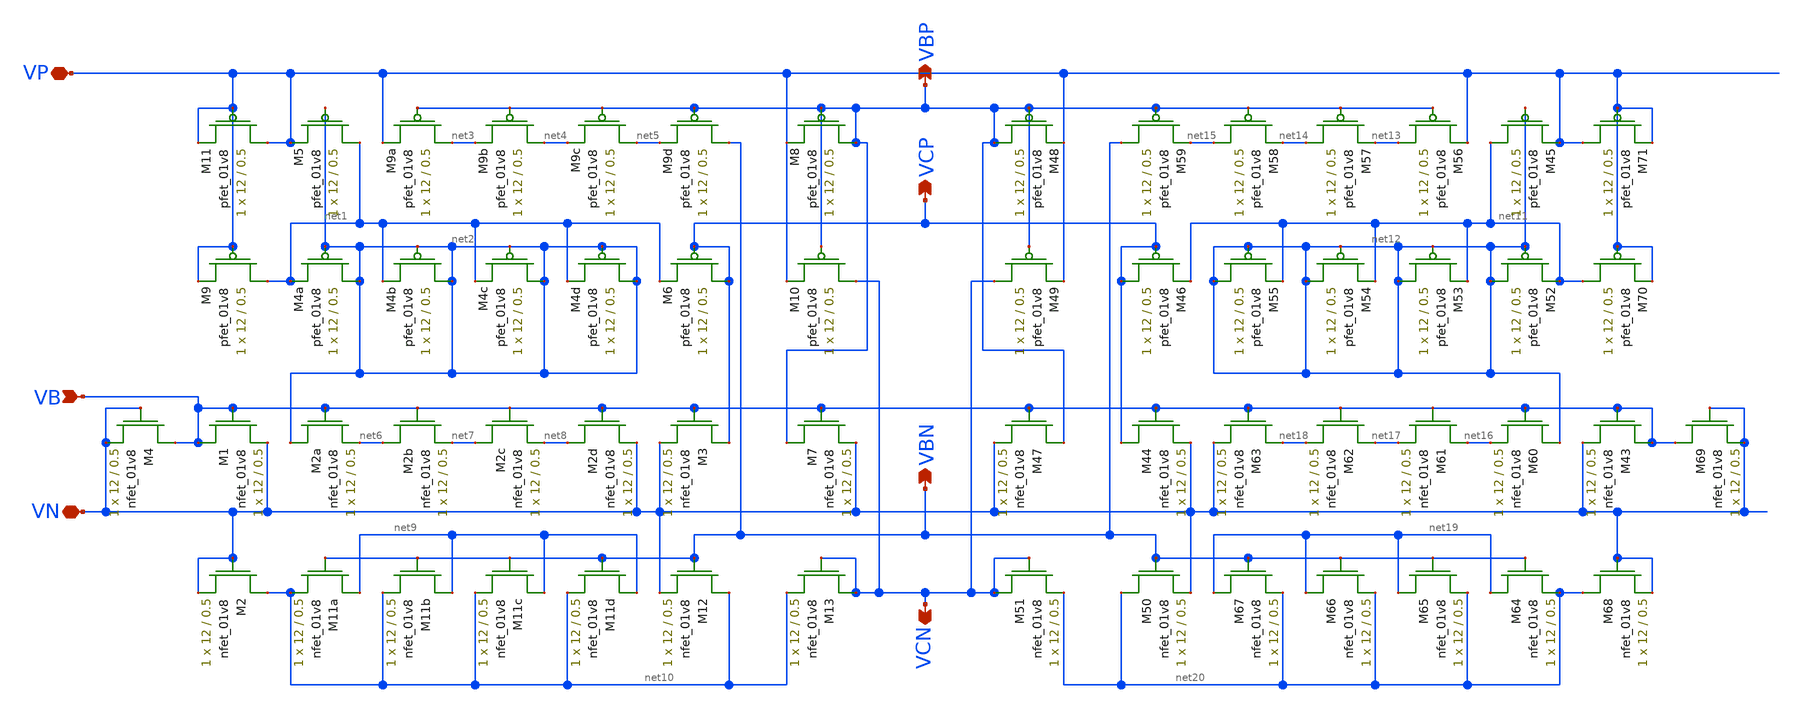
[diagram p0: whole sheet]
** sch_path: mp3/bias_gen/bias_gen_LDS_v2.sch
**.subckt bias_gen_LDS_v2 VN VP VCN VCP VBP VB VBN
*.iopin VN
*.iopin VP
*.opin VCN
*.opin VCP
*.opin VBP
*.ipin VB
*.opin VBN
XM1 VB VB VN VN sky130_fd_pr__nfet_01v8 L=0.5 W=12 nf=1 ad='int((nf+1)/2) * W/nf * 0.29' as='int((nf+2)/2) * W/nf * 0.29'
+ pd='2*int((nf+1)/2) * (W/nf + 0.29)' ps='2*int((nf+2)/2) * (W/nf + 0.29)' nrd='0.29 / W' nrs='0.29 / W'
+ sa=0 sb=0 sd=0 mult=1 m=1
XM3 VCP VB VN VN sky130_fd_pr__nfet_01v8 L=0.5 W=12 nf=1 ad='int((nf+1)/2) * W/nf * 0.29' as='int((nf+2)/2) * W/nf * 0.29'
+ pd='2*int((nf+1)/2) * (W/nf + 0.29)' ps='2*int((nf+2)/2) * (W/nf + 0.29)' nrd='0.29 / W' nrs='0.29 / W'
+ sa=0 sb=0 sd=0 mult=1 m=1
XM5 net1 net2 VP VP sky130_fd_pr__pfet_01v8 L=0.5 W=12 nf=1 ad='int((nf+1)/2) * W/nf * 0.29' as='int((nf+2)/2) * W/nf * 0.29'
+ pd='2*int((nf+1)/2) * (W/nf + 0.29)' ps='2*int((nf+2)/2) * (W/nf + 0.29)' nrd='0.29 / W' nrs='0.29 / W'
+ sa=0 sb=0 sd=0 mult=1 m=1
XM6 VCP VCP net1 VP sky130_fd_pr__pfet_01v8 L=0.5 W=12 nf=1 ad='int((nf+1)/2) * W/nf * 0.29' as='int((nf+2)/2) * W/nf * 0.29'
+ pd='2*int((nf+1)/2) * (W/nf + 0.29)' ps='2*int((nf+2)/2) * (W/nf + 0.29)' nrd='0.29 / W' nrs='0.29 / W'
+ sa=0 sb=0 sd=0 mult=1 m=1
XM7 VBP VB VN VN sky130_fd_pr__nfet_01v8 L=0.5 W=12 nf=1 ad='int((nf+1)/2) * W/nf * 0.29' as='int((nf+2)/2) * W/nf * 0.29'
+ pd='2*int((nf+1)/2) * (W/nf + 0.29)' ps='2*int((nf+2)/2) * (W/nf + 0.29)' nrd='0.29 / W' nrs='0.29 / W'
+ sa=0 sb=0 sd=0 mult=1 m=1
XM8 VBP VBP VP VP sky130_fd_pr__pfet_01v8 L=0.5 W=12 nf=1 ad='int((nf+1)/2) * W/nf * 0.29' as='int((nf+2)/2) * W/nf * 0.29'
+ pd='2*int((nf+1)/2) * (W/nf + 0.29)' ps='2*int((nf+2)/2) * (W/nf + 0.29)' nrd='0.29 / W' nrs='0.29 / W'
+ sa=0 sb=0 sd=0 mult=1 m=1
XM10 VCN VBP VP VP sky130_fd_pr__pfet_01v8 L=0.5 W=12 nf=1 ad='int((nf+1)/2) * W/nf * 0.29' as='int((nf+2)/2) * W/nf * 0.29'
+ pd='2*int((nf+1)/2) * (W/nf + 0.29)' ps='2*int((nf+2)/2) * (W/nf + 0.29)' nrd='0.29 / W' nrs='0.29 / W'
+ sa=0 sb=0 sd=0 mult=1 m=1
XM12 net10 VBN VN VN sky130_fd_pr__nfet_01v8 L=0.5 W=12 nf=1 ad='int((nf+1)/2) * W/nf * 0.29' as='int((nf+2)/2) * W/nf * 0.29'
+ pd='2*int((nf+1)/2) * (W/nf + 0.29)' ps='2*int((nf+2)/2) * (W/nf + 0.29)' nrd='0.29 / W' nrs='0.29 / W'
+ sa=0 sb=0 sd=0 mult=1 m=1
XM13 VCN VCN net10 VN sky130_fd_pr__nfet_01v8 L=0.5 W=12 nf=1 ad='int((nf+1)/2) * W/nf * 0.29' as='int((nf+2)/2) * W/nf * 0.29'
+ pd='2*int((nf+1)/2) * (W/nf + 0.29)' ps='2*int((nf+2)/2) * (W/nf + 0.29)' nrd='0.29 / W' nrs='0.29 / W'
+ sa=0 sb=0 sd=0 mult=1 m=1
XM4a net2 net2 net1 VP sky130_fd_pr__pfet_01v8 L=0.5 W=12 nf=1 ad='int((nf+1)/2) * W/nf * 0.29' as='int((nf+2)/2) * W/nf * 0.29'
+ pd='2*int((nf+1)/2) * (W/nf + 0.29)' ps='2*int((nf+2)/2) * (W/nf + 0.29)' nrd='0.29 / W' nrs='0.29 / W'
+ sa=0 sb=0 sd=0 mult=1 m=1
XM4b net2 net2 net1 VP sky130_fd_pr__pfet_01v8 L=0.5 W=12 nf=1 ad='int((nf+1)/2) * W/nf * 0.29' as='int((nf+2)/2) * W/nf * 0.29'
+ pd='2*int((nf+1)/2) * (W/nf + 0.29)' ps='2*int((nf+2)/2) * (W/nf + 0.29)' nrd='0.29 / W' nrs='0.29 / W'
+ sa=0 sb=0 sd=0 mult=1 m=1
XM4c net2 net2 net1 VP sky130_fd_pr__pfet_01v8 L=0.5 W=12 nf=1 ad='int((nf+1)/2) * W/nf * 0.29' as='int((nf+2)/2) * W/nf * 0.29'
+ pd='2*int((nf+1)/2) * (W/nf + 0.29)' ps='2*int((nf+2)/2) * (W/nf + 0.29)' nrd='0.29 / W' nrs='0.29 / W'
+ sa=0 sb=0 sd=0 mult=1 m=1
XM4d net2 net2 net1 VP sky130_fd_pr__pfet_01v8 L=0.5 W=12 nf=1 ad='int((nf+1)/2) * W/nf * 0.29' as='int((nf+2)/2) * W/nf * 0.29'
+ pd='2*int((nf+1)/2) * (W/nf + 0.29)' ps='2*int((nf+2)/2) * (W/nf + 0.29)' nrd='0.29 / W' nrs='0.29 / W'
+ sa=0 sb=0 sd=0 mult=1 m=1
XM9a net3 VBP VP VP sky130_fd_pr__pfet_01v8 L=0.5 W=12 nf=1 ad='int((nf+1)/2) * W/nf * 0.29' as='int((nf+2)/2) * W/nf * 0.29'
+ pd='2*int((nf+1)/2) * (W/nf + 0.29)' ps='2*int((nf+2)/2) * (W/nf + 0.29)' nrd='0.29 / W' nrs='0.29 / W'
+ sa=0 sb=0 sd=0 mult=1 m=1
XM9b net4 VBP net3 VP sky130_fd_pr__pfet_01v8 L=0.5 W=12 nf=1 ad='int((nf+1)/2) * W/nf * 0.29' as='int((nf+2)/2) * W/nf * 0.29'
+ pd='2*int((nf+1)/2) * (W/nf + 0.29)' ps='2*int((nf+2)/2) * (W/nf + 0.29)' nrd='0.29 / W' nrs='0.29 / W'
+ sa=0 sb=0 sd=0 mult=1 m=1
XM9c net5 VBP net4 VP sky130_fd_pr__pfet_01v8 L=0.5 W=12 nf=1 ad='int((nf+1)/2) * W/nf * 0.29' as='int((nf+2)/2) * W/nf * 0.29'
+ pd='2*int((nf+1)/2) * (W/nf + 0.29)' ps='2*int((nf+2)/2) * (W/nf + 0.29)' nrd='0.29 / W' nrs='0.29 / W'
+ sa=0 sb=0 sd=0 mult=1 m=1
XM9d VBN VBP net5 VP sky130_fd_pr__pfet_01v8 L=0.5 W=12 nf=1 ad='int((nf+1)/2) * W/nf * 0.29' as='int((nf+2)/2) * W/nf * 0.29'
+ pd='2*int((nf+1)/2) * (W/nf + 0.29)' ps='2*int((nf+2)/2) * (W/nf + 0.29)' nrd='0.29 / W' nrs='0.29 / W'
+ sa=0 sb=0 sd=0 mult=1 m=1
XM2a net2 VB net6 VN sky130_fd_pr__nfet_01v8 L=0.5 W=12 nf=1 ad='int((nf+1)/2) * W/nf * 0.29' as='int((nf+2)/2) * W/nf * 0.29'
+ pd='2*int((nf+1)/2) * (W/nf + 0.29)' ps='2*int((nf+2)/2) * (W/nf + 0.29)' nrd='0.29 / W' nrs='0.29 / W'
+ sa=0 sb=0 sd=0 mult=1 m=1
XM2b net6 VB net7 VN sky130_fd_pr__nfet_01v8 L=0.5 W=12 nf=1 ad='int((nf+1)/2) * W/nf * 0.29' as='int((nf+2)/2) * W/nf * 0.29'
+ pd='2*int((nf+1)/2) * (W/nf + 0.29)' ps='2*int((nf+2)/2) * (W/nf + 0.29)' nrd='0.29 / W' nrs='0.29 / W'
+ sa=0 sb=0 sd=0 mult=1 m=1
XM2c net7 VB net8 VN sky130_fd_pr__nfet_01v8 L=0.5 W=12 nf=1 ad='int((nf+1)/2) * W/nf * 0.29' as='int((nf+2)/2) * W/nf * 0.29'
+ pd='2*int((nf+1)/2) * (W/nf + 0.29)' ps='2*int((nf+2)/2) * (W/nf + 0.29)' nrd='0.29 / W' nrs='0.29 / W'
+ sa=0 sb=0 sd=0 mult=1 m=1
XM2d net8 VB VN VN sky130_fd_pr__nfet_01v8 L=0.5 W=12 nf=1 ad='int((nf+1)/2) * W/nf * 0.29' as='int((nf+2)/2) * W/nf * 0.29'
+ pd='2*int((nf+1)/2) * (W/nf + 0.29)' ps='2*int((nf+2)/2) * (W/nf + 0.29)' nrd='0.29 / W' nrs='0.29 / W'
+ sa=0 sb=0 sd=0 mult=1 m=1
XM11a net9 VBN net10 VN sky130_fd_pr__nfet_01v8 L=0.5 W=12 nf=1 ad='int((nf+1)/2) * W/nf * 0.29' as='int((nf+2)/2) * W/nf * 0.29'
+ pd='2*int((nf+1)/2) * (W/nf + 0.29)' ps='2*int((nf+2)/2) * (W/nf + 0.29)' nrd='0.29 / W' nrs='0.29 / W'
+ sa=0 sb=0 sd=0 mult=1 m=1
XM11b net9 VBN net10 VN sky130_fd_pr__nfet_01v8 L=0.5 W=12 nf=1 ad='int((nf+1)/2) * W/nf * 0.29' as='int((nf+2)/2) * W/nf * 0.29'
+ pd='2*int((nf+1)/2) * (W/nf + 0.29)' ps='2*int((nf+2)/2) * (W/nf + 0.29)' nrd='0.29 / W' nrs='0.29 / W'
+ sa=0 sb=0 sd=0 mult=1 m=1
XM11c net9 VBN net10 VN sky130_fd_pr__nfet_01v8 L=0.5 W=12 nf=1 ad='int((nf+1)/2) * W/nf * 0.29' as='int((nf+2)/2) * W/nf * 0.29'
+ pd='2*int((nf+1)/2) * (W/nf + 0.29)' ps='2*int((nf+2)/2) * (W/nf + 0.29)' nrd='0.29 / W' nrs='0.29 / W'
+ sa=0 sb=0 sd=0 mult=1 m=1
XM11d net9 VBN net10 VN sky130_fd_pr__nfet_01v8 L=0.5 W=12 nf=1 ad='int((nf+1)/2) * W/nf * 0.29' as='int((nf+2)/2) * W/nf * 0.29'
+ pd='2*int((nf+1)/2) * (W/nf + 0.29)' ps='2*int((nf+2)/2) * (W/nf + 0.29)' nrd='0.29 / W' nrs='0.29 / W'
+ sa=0 sb=0 sd=0 mult=1 m=1
XM2 net10 VN VN VN sky130_fd_pr__nfet_01v8 L=0.5 W=12 nf=1 ad='int((nf+1)/2) * W/nf * 0.29' as='int((nf+2)/2) * W/nf * 0.29'
+ pd='2*int((nf+1)/2) * (W/nf + 0.29)' ps='2*int((nf+2)/2) * (W/nf + 0.29)' nrd='0.29 / W' nrs='0.29 / W'
+ sa=0 sb=0 sd=0 mult=1 m=1
XM4 VB VN VN VN sky130_fd_pr__nfet_01v8 L=0.5 W=12 nf=1 ad='int((nf+1)/2) * W/nf * 0.29' as='int((nf+2)/2) * W/nf * 0.29'
+ pd='2*int((nf+1)/2) * (W/nf + 0.29)' ps='2*int((nf+2)/2) * (W/nf + 0.29)' nrd='0.29 / W' nrs='0.29 / W'
+ sa=0 sb=0 sd=0 mult=1 m=1
XM9 net1 VP VP VP sky130_fd_pr__pfet_01v8 L=0.5 W=12 nf=1 ad='int((nf+1)/2) * W/nf * 0.29' as='int((nf+2)/2) * W/nf * 0.29'
+ pd='2*int((nf+1)/2) * (W/nf + 0.29)' ps='2*int((nf+2)/2) * (W/nf + 0.29)' nrd='0.29 / W' nrs='0.29 / W'
+ sa=0 sb=0 sd=0 mult=1 m=1
XM11 VP VP VP VP sky130_fd_pr__pfet_01v8 L=0.5 W=12 nf=1 ad='int((nf+1)/2) * W/nf * 0.29' as='int((nf+2)/2) * W/nf * 0.29'
+ pd='2*int((nf+1)/2) * (W/nf + 0.29)' ps='2*int((nf+2)/2) * (W/nf + 0.29)' nrd='0.29 / W' nrs='0.29 / W'
+ sa=0 sb=0 sd=0 mult=1 m=1
XM43 VB VB VN VN sky130_fd_pr__nfet_01v8 L=0.5 W=12 nf=1 ad='int((nf+1)/2) * W/nf * 0.29' as='int((nf+2)/2) * W/nf * 0.29'
+ pd='2*int((nf+1)/2) * (W/nf + 0.29)' ps='2*int((nf+2)/2) * (W/nf + 0.29)' nrd='0.29 / W' nrs='0.29 / W'
+ sa=0 sb=0 sd=0 mult=1 m=1
XM44 VCP VB VN VN sky130_fd_pr__nfet_01v8 L=0.5 W=12 nf=1 ad='int((nf+1)/2) * W/nf * 0.29' as='int((nf+2)/2) * W/nf * 0.29'
+ pd='2*int((nf+1)/2) * (W/nf + 0.29)' ps='2*int((nf+2)/2) * (W/nf + 0.29)' nrd='0.29 / W' nrs='0.29 / W'
+ sa=0 sb=0 sd=0 mult=1 m=1
XM45 net11 net12 VP VP sky130_fd_pr__pfet_01v8 L=0.5 W=12 nf=1 ad='int((nf+1)/2) * W/nf * 0.29' as='int((nf+2)/2) * W/nf * 0.29'
+ pd='2*int((nf+1)/2) * (W/nf + 0.29)' ps='2*int((nf+2)/2) * (W/nf + 0.29)' nrd='0.29 / W' nrs='0.29 / W'
+ sa=0 sb=0 sd=0 mult=1 m=1
XM46 VCP VCP net11 VP sky130_fd_pr__pfet_01v8 L=0.5 W=12 nf=1 ad='int((nf+1)/2) * W/nf * 0.29' as='int((nf+2)/2) * W/nf * 0.29'
+ pd='2*int((nf+1)/2) * (W/nf + 0.29)' ps='2*int((nf+2)/2) * (W/nf + 0.29)' nrd='0.29 / W' nrs='0.29 / W'
+ sa=0 sb=0 sd=0 mult=1 m=1
XM47 VBP VB VN VN sky130_fd_pr__nfet_01v8 L=0.5 W=12 nf=1 ad='int((nf+1)/2) * W/nf * 0.29' as='int((nf+2)/2) * W/nf * 0.29'
+ pd='2*int((nf+1)/2) * (W/nf + 0.29)' ps='2*int((nf+2)/2) * (W/nf + 0.29)' nrd='0.29 / W' nrs='0.29 / W'
+ sa=0 sb=0 sd=0 mult=1 m=1
XM48 VBP VBP VP VP sky130_fd_pr__pfet_01v8 L=0.5 W=12 nf=1 ad='int((nf+1)/2) * W/nf * 0.29' as='int((nf+2)/2) * W/nf * 0.29'
+ pd='2*int((nf+1)/2) * (W/nf + 0.29)' ps='2*int((nf+2)/2) * (W/nf + 0.29)' nrd='0.29 / W' nrs='0.29 / W'
+ sa=0 sb=0 sd=0 mult=1 m=1
XM49 VCN VBP VP VP sky130_fd_pr__pfet_01v8 L=0.5 W=12 nf=1 ad='int((nf+1)/2) * W/nf * 0.29' as='int((nf+2)/2) * W/nf * 0.29'
+ pd='2*int((nf+1)/2) * (W/nf + 0.29)' ps='2*int((nf+2)/2) * (W/nf + 0.29)' nrd='0.29 / W' nrs='0.29 / W'
+ sa=0 sb=0 sd=0 mult=1 m=1
XM50 net20 VBN VN VN sky130_fd_pr__nfet_01v8 L=0.5 W=12 nf=1 ad='int((nf+1)/2) * W/nf * 0.29' as='int((nf+2)/2) * W/nf * 0.29'
+ pd='2*int((nf+1)/2) * (W/nf + 0.29)' ps='2*int((nf+2)/2) * (W/nf + 0.29)' nrd='0.29 / W' nrs='0.29 / W'
+ sa=0 sb=0 sd=0 mult=1 m=1
XM51 VCN VCN net20 VN sky130_fd_pr__nfet_01v8 L=0.5 W=12 nf=1 ad='int((nf+1)/2) * W/nf * 0.29' as='int((nf+2)/2) * W/nf * 0.29'
+ pd='2*int((nf+1)/2) * (W/nf + 0.29)' ps='2*int((nf+2)/2) * (W/nf + 0.29)' nrd='0.29 / W' nrs='0.29 / W'
+ sa=0 sb=0 sd=0 mult=1 m=1
XM52 net12 net12 net11 VP sky130_fd_pr__pfet_01v8 L=0.5 W=12 nf=1 ad='int((nf+1)/2) * W/nf * 0.29' as='int((nf+2)/2) * W/nf * 0.29'
+ pd='2*int((nf+1)/2) * (W/nf + 0.29)' ps='2*int((nf+2)/2) * (W/nf + 0.29)' nrd='0.29 / W' nrs='0.29 / W'
+ sa=0 sb=0 sd=0 mult=1 m=1
XM53 net12 net12 net11 VP sky130_fd_pr__pfet_01v8 L=0.5 W=12 nf=1 ad='int((nf+1)/2) * W/nf * 0.29' as='int((nf+2)/2) * W/nf * 0.29'
+ pd='2*int((nf+1)/2) * (W/nf + 0.29)' ps='2*int((nf+2)/2) * (W/nf + 0.29)' nrd='0.29 / W' nrs='0.29 / W'
+ sa=0 sb=0 sd=0 mult=1 m=1
XM54 net12 net12 net11 VP sky130_fd_pr__pfet_01v8 L=0.5 W=12 nf=1 ad='int((nf+1)/2) * W/nf * 0.29' as='int((nf+2)/2) * W/nf * 0.29'
+ pd='2*int((nf+1)/2) * (W/nf + 0.29)' ps='2*int((nf+2)/2) * (W/nf + 0.29)' nrd='0.29 / W' nrs='0.29 / W'
+ sa=0 sb=0 sd=0 mult=1 m=1
XM55 net12 net12 net11 VP sky130_fd_pr__pfet_01v8 L=0.5 W=12 nf=1 ad='int((nf+1)/2) * W/nf * 0.29' as='int((nf+2)/2) * W/nf * 0.29'
+ pd='2*int((nf+1)/2) * (W/nf + 0.29)' ps='2*int((nf+2)/2) * (W/nf + 0.29)' nrd='0.29 / W' nrs='0.29 / W'
+ sa=0 sb=0 sd=0 mult=1 m=1
XM56 net13 VBP VP VP sky130_fd_pr__pfet_01v8 L=0.5 W=12 nf=1 ad='int((nf+1)/2) * W/nf * 0.29' as='int((nf+2)/2) * W/nf * 0.29'
+ pd='2*int((nf+1)/2) * (W/nf + 0.29)' ps='2*int((nf+2)/2) * (W/nf + 0.29)' nrd='0.29 / W' nrs='0.29 / W'
+ sa=0 sb=0 sd=0 mult=1 m=1
XM57 net14 VBP net13 VP sky130_fd_pr__pfet_01v8 L=0.5 W=12 nf=1 ad='int((nf+1)/2) * W/nf * 0.29' as='int((nf+2)/2) * W/nf * 0.29'
+ pd='2*int((nf+1)/2) * (W/nf + 0.29)' ps='2*int((nf+2)/2) * (W/nf + 0.29)' nrd='0.29 / W' nrs='0.29 / W'
+ sa=0 sb=0 sd=0 mult=1 m=1
XM58 net15 VBP net14 VP sky130_fd_pr__pfet_01v8 L=0.5 W=12 nf=1 ad='int((nf+1)/2) * W/nf * 0.29' as='int((nf+2)/2) * W/nf * 0.29'
+ pd='2*int((nf+1)/2) * (W/nf + 0.29)' ps='2*int((nf+2)/2) * (W/nf + 0.29)' nrd='0.29 / W' nrs='0.29 / W'
+ sa=0 sb=0 sd=0 mult=1 m=1
XM59 VBN VBP net15 VP sky130_fd_pr__pfet_01v8 L=0.5 W=12 nf=1 ad='int((nf+1)/2) * W/nf * 0.29' as='int((nf+2)/2) * W/nf * 0.29'
+ pd='2*int((nf+1)/2) * (W/nf + 0.29)' ps='2*int((nf+2)/2) * (W/nf + 0.29)' nrd='0.29 / W' nrs='0.29 / W'
+ sa=0 sb=0 sd=0 mult=1 m=1
XM60 net12 VB net16 VN sky130_fd_pr__nfet_01v8 L=0.5 W=12 nf=1 ad='int((nf+1)/2) * W/nf * 0.29' as='int((nf+2)/2) * W/nf * 0.29'
+ pd='2*int((nf+1)/2) * (W/nf + 0.29)' ps='2*int((nf+2)/2) * (W/nf + 0.29)' nrd='0.29 / W' nrs='0.29 / W'
+ sa=0 sb=0 sd=0 mult=1 m=1
XM61 net16 VB net17 VN sky130_fd_pr__nfet_01v8 L=0.5 W=12 nf=1 ad='int((nf+1)/2) * W/nf * 0.29' as='int((nf+2)/2) * W/nf * 0.29'
+ pd='2*int((nf+1)/2) * (W/nf + 0.29)' ps='2*int((nf+2)/2) * (W/nf + 0.29)' nrd='0.29 / W' nrs='0.29 / W'
+ sa=0 sb=0 sd=0 mult=1 m=1
XM62 net17 VB net18 VN sky130_fd_pr__nfet_01v8 L=0.5 W=12 nf=1 ad='int((nf+1)/2) * W/nf * 0.29' as='int((nf+2)/2) * W/nf * 0.29'
+ pd='2*int((nf+1)/2) * (W/nf + 0.29)' ps='2*int((nf+2)/2) * (W/nf + 0.29)' nrd='0.29 / W' nrs='0.29 / W'
+ sa=0 sb=0 sd=0 mult=1 m=1
XM63 net18 VB VN VN sky130_fd_pr__nfet_01v8 L=0.5 W=12 nf=1 ad='int((nf+1)/2) * W/nf * 0.29' as='int((nf+2)/2) * W/nf * 0.29'
+ pd='2*int((nf+1)/2) * (W/nf + 0.29)' ps='2*int((nf+2)/2) * (W/nf + 0.29)' nrd='0.29 / W' nrs='0.29 / W'
+ sa=0 sb=0 sd=0 mult=1 m=1
XM64 net19 VBN net20 VN sky130_fd_pr__nfet_01v8 L=0.5 W=12 nf=1 ad='int((nf+1)/2) * W/nf * 0.29' as='int((nf+2)/2) * W/nf * 0.29'
+ pd='2*int((nf+1)/2) * (W/nf + 0.29)' ps='2*int((nf+2)/2) * (W/nf + 0.29)' nrd='0.29 / W' nrs='0.29 / W'
+ sa=0 sb=0 sd=0 mult=1 m=1
XM65 net19 VBN net20 VN sky130_fd_pr__nfet_01v8 L=0.5 W=12 nf=1 ad='int((nf+1)/2) * W/nf * 0.29' as='int((nf+2)/2) * W/nf * 0.29'
+ pd='2*int((nf+1)/2) * (W/nf + 0.29)' ps='2*int((nf+2)/2) * (W/nf + 0.29)' nrd='0.29 / W' nrs='0.29 / W'
+ sa=0 sb=0 sd=0 mult=1 m=1
XM66 net19 VBN net20 VN sky130_fd_pr__nfet_01v8 L=0.5 W=12 nf=1 ad='int((nf+1)/2) * W/nf * 0.29' as='int((nf+2)/2) * W/nf * 0.29'
+ pd='2*int((nf+1)/2) * (W/nf + 0.29)' ps='2*int((nf+2)/2) * (W/nf + 0.29)' nrd='0.29 / W' nrs='0.29 / W'
+ sa=0 sb=0 sd=0 mult=1 m=1
XM67 net19 VBN net20 VN sky130_fd_pr__nfet_01v8 L=0.5 W=12 nf=1 ad='int((nf+1)/2) * W/nf * 0.29' as='int((nf+2)/2) * W/nf * 0.29'
+ pd='2*int((nf+1)/2) * (W/nf + 0.29)' ps='2*int((nf+2)/2) * (W/nf + 0.29)' nrd='0.29 / W' nrs='0.29 / W'
+ sa=0 sb=0 sd=0 mult=1 m=1
XM68 net20 VN VN VN sky130_fd_pr__nfet_01v8 L=0.5 W=12 nf=1 ad='int((nf+1)/2) * W/nf * 0.29' as='int((nf+2)/2) * W/nf * 0.29'
+ pd='2*int((nf+1)/2) * (W/nf + 0.29)' ps='2*int((nf+2)/2) * (W/nf + 0.29)' nrd='0.29 / W' nrs='0.29 / W'
+ sa=0 sb=0 sd=0 mult=1 m=1
XM69 VB VN VN VN sky130_fd_pr__nfet_01v8 L=0.5 W=12 nf=1 ad='int((nf+1)/2) * W/nf * 0.29' as='int((nf+2)/2) * W/nf * 0.29'
+ pd='2*int((nf+1)/2) * (W/nf + 0.29)' ps='2*int((nf+2)/2) * (W/nf + 0.29)' nrd='0.29 / W' nrs='0.29 / W'
+ sa=0 sb=0 sd=0 mult=1 m=1
XM70 net11 VP VP VP sky130_fd_pr__pfet_01v8 L=0.5 W=12 nf=1 ad='int((nf+1)/2) * W/nf * 0.29' as='int((nf+2)/2) * W/nf * 0.29'
+ pd='2*int((nf+1)/2) * (W/nf + 0.29)' ps='2*int((nf+2)/2) * (W/nf + 0.29)' nrd='0.29 / W' nrs='0.29 / W'
+ sa=0 sb=0 sd=0 mult=1 m=1
XM71 VP VP VP VP sky130_fd_pr__pfet_01v8 L=0.5 W=12 nf=1 ad='int((nf+1)/2) * W/nf * 0.29' as='int((nf+2)/2) * W/nf * 0.29'
+ pd='2*int((nf+1)/2) * (W/nf + 0.29)' ps='2*int((nf+2)/2) * (W/nf + 0.29)' nrd='0.29 / W' nrs='0.29 / W'
+ sa=0 sb=0 sd=0 mult=1 m=1
**.ends
.end
